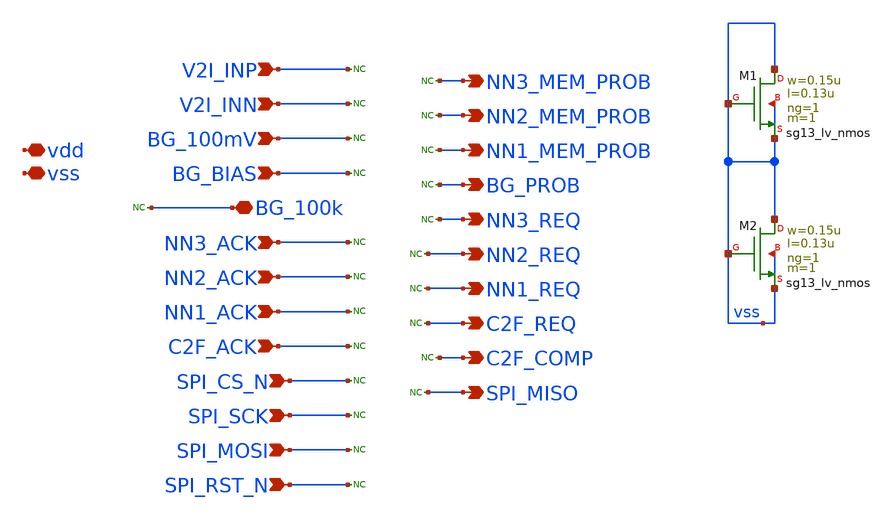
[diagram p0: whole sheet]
** sch_path: v2_feature_extr_withf/INI_Block_Arianna.sch
**.subckt INI_Block_Arianna vdd vss V2I_INP V2I_INN BG_100mV BG_BIAS BG_100k NN3_ACK NN2_ACK NN1_ACK
*+ C2F_ACK SPI_CS_N SPI_SCK SPI_MOSI SPI_RST_N NN3_MEM_PROB NN2_MEM_PROB NN1_MEM_PROB BG_PROB NN3_REQ NN2_REQ
*+ NN1_REQ C2F_REQ C2F_COMP SPI_MISO
*.iopin vdd
*.iopin vss
*.ipin V2I_INP
*.ipin V2I_INN
*.ipin BG_100mV
*.ipin BG_BIAS
*.iopin BG_100k
*.ipin NN3_ACK
*.ipin NN2_ACK
*.ipin NN1_ACK
*.ipin C2F_ACK
*.ipin SPI_CS_N
*.ipin SPI_SCK
*.ipin SPI_MOSI
*.ipin SPI_RST_N
*.opin NN3_MEM_PROB
*.opin NN2_MEM_PROB
*.opin NN1_MEM_PROB
*.opin BG_PROB
*.opin NN3_REQ
*.opin NN2_REQ
*.opin NN1_REQ
*.opin C2F_REQ
*.opin C2F_COMP
*.opin SPI_MISO
XM1 vss vss vss vss sg13_lv_nmos w=0.15u l=0.13u ng=1 m=1 mm_ok=1
XM2 vss vss vss vss sg13_lv_nmos w=0.15u l=0.13u ng=1 m=1 mm_ok=1
* noconn V2I_INP
* noconn V2I_INN
* noconn BG_100mV
* noconn BG_BIAS
* noconn NN3_ACK
* noconn NN2_ACK
* noconn NN1_ACK
* noconn C2F_ACK
* noconn SPI_CS_N
* noconn SPI_SCK
* noconn SPI_MOSI
* noconn SPI_RST_N
* noconn BG_100k
* noconn NN3_MEM_PROB
* noconn NN2_MEM_PROB
* noconn NN1_MEM_PROB
* noconn BG_PROB
* noconn NN3_REQ
* noconn NN2_REQ
* noconn NN1_REQ
* noconn C2F_REQ
* noconn C2F_COMP
* noconn SPI_MISO
**.ends
.end
